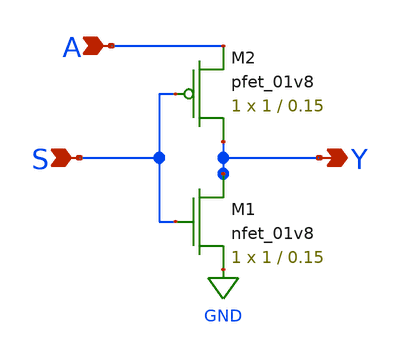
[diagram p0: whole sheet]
** sch_path: dac/schematics/misc/untitled.sch
**.subckt untitled S A Y
*.ipin S
*.ipin A
*.opin Y
XM1 Y S GND GND sky130_fd_pr__nfet_01v8 L=0.15 W=1 nf=1 ad='int((nf+1)/2) * W/nf * 0.29' as='int((nf+2)/2) * W/nf * 0.29'
+ pd='2*int((nf+1)/2) * (W/nf + 0.29)' ps='2*int((nf+2)/2) * (W/nf + 0.29)' nrd='0.29 / W' nrs='0.29 / W'
+ sa=0 sb=0 sd=0 mult=1 m=1
XM2 Y S A VDD sky130_fd_pr__pfet_01v8 L=0.15 W=1 nf=1 ad='int((nf+1)/2) * W/nf * 0.29' as='int((nf+2)/2) * W/nf * 0.29'
+ pd='2*int((nf+1)/2) * (W/nf + 0.29)' ps='2*int((nf+2)/2) * (W/nf + 0.29)' nrd='0.29 / W' nrs='0.29 / W'
+ sa=0 sb=0 sd=0 mult=1 m=1
**.ends
.GLOBAL GND
.end
